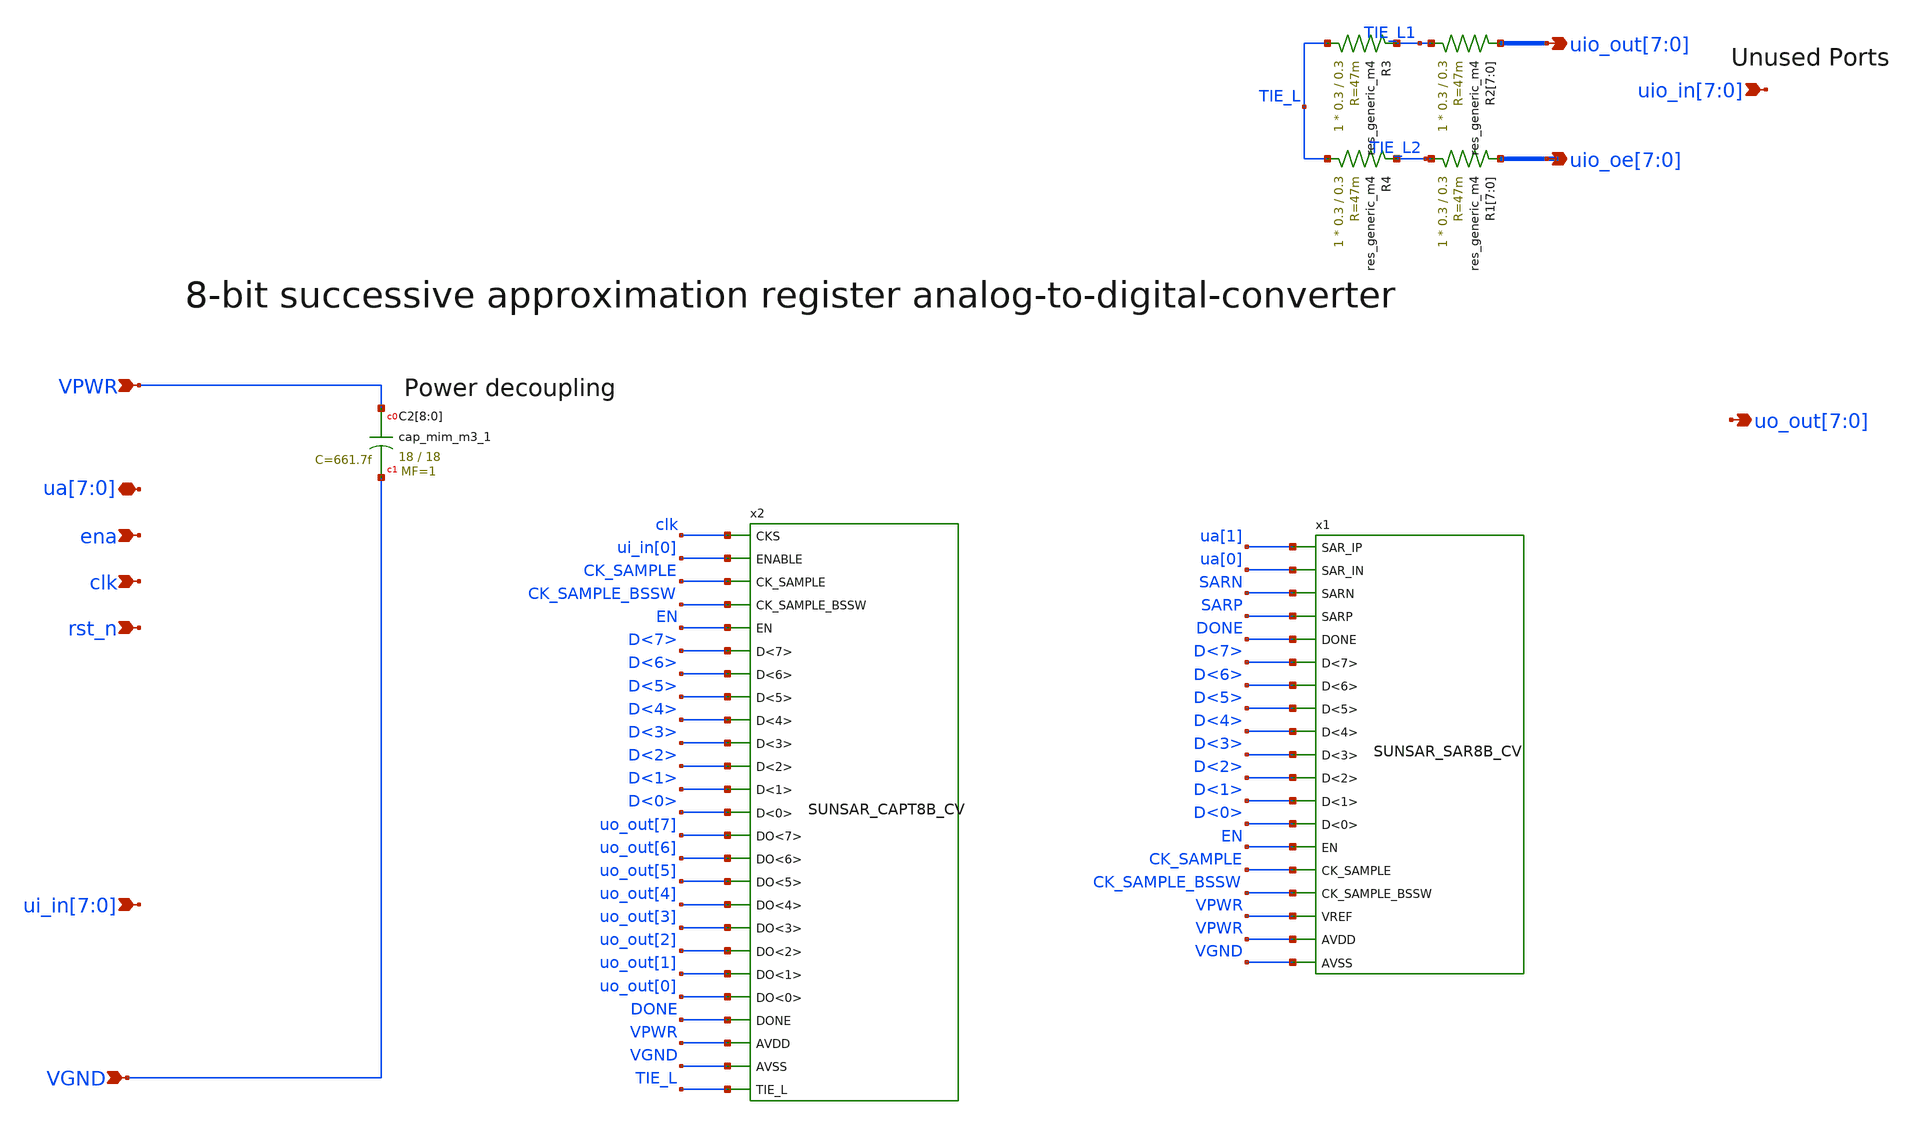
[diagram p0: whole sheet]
** sch_path: ip/tt06_sar_sky130nm/design/TT06_SAR_SKY130NM/tt_um_TT06_SAR_wulffern.sch
**.subckt tt_um_TT06_SAR_wulffern VPWR VGND
*+ ui_in[7],ui_in[6],ui_in[5],ui_in[4],ui_in[3],ui_in[2],ui_in[1],ui_in[0] uo_out[7],uo_out[6],uo_out[5],uo_out[4],uo_out[3],uo_out[2],uo_out[1],uo_out[0]
*+ uio_in[7],uio_in[6],uio_in[5],uio_in[4],uio_in[3],uio_in[2],uio_in[1],uio_in[0] uio_out[7],uio_out[6],uio_out[5],uio_out[4],uio_out[3],uio_out[2],uio_out[1],uio_out[0]
*+ uio_oe[7],uio_oe[6],uio_oe[5],uio_oe[4],uio_oe[3],uio_oe[2],uio_oe[1],uio_oe[0] ua[7],ua[6],ua[5],ua[4],ua[3],ua[2],ua[1],ua[0] ena clk rst_n
*.ipin VPWR
*.ipin VGND
*.ipin ui_in[7],ui_in[6],ui_in[5],ui_in[4],ui_in[3],ui_in[2],ui_in[1],ui_in[0]
*.opin uo_out[7],uo_out[6],uo_out[5],uo_out[4],uo_out[3],uo_out[2],uo_out[1],uo_out[0]
*.ipin uio_in[7],uio_in[6],uio_in[5],uio_in[4],uio_in[3],uio_in[2],uio_in[1],uio_in[0]
*.opin uio_out[7],uio_out[6],uio_out[5],uio_out[4],uio_out[3],uio_out[2],uio_out[1],uio_out[0]
*.opin uio_oe[7],uio_oe[6],uio_oe[5],uio_oe[4],uio_oe[3],uio_oe[2],uio_oe[1],uio_oe[0]
*.iopin ua[7],ua[6],ua[5],ua[4],ua[3],ua[2],ua[1],ua[0]
*.ipin ena
*.ipin clk
*.ipin rst_n
x1 ua[1] ua[0] SARN SARP DONE D<7> D<6> D<5> D<4> D<3> D<2> D<1> D<0> EN CK_SAMPLE CK_SAMPLE_BSSW
+ VPWR VPWR VGND SUNSAR_SAR8B_CV
x2 clk ui_in[0] CK_SAMPLE CK_SAMPLE_BSSW EN D<7> D<6> D<5> D<4> D<3> D<2> D<1> D<0> uo_out[7]
+ uo_out[6] uo_out[5] uo_out[4] uo_out[3] uo_out[2] uo_out[1] uo_out[0] DONE VPWR VGND TIE_L SUNSAR_CAPT8B_CV
R1[7] TIE_L2 uio_oe[7] sky130_fd_pr__res_generic_m4 W=0.3 L=0.3 m=1
R1[6] TIE_L2 uio_oe[6] sky130_fd_pr__res_generic_m4 W=0.3 L=0.3 m=1
R1[5] TIE_L2 uio_oe[5] sky130_fd_pr__res_generic_m4 W=0.3 L=0.3 m=1
R1[4] TIE_L2 uio_oe[4] sky130_fd_pr__res_generic_m4 W=0.3 L=0.3 m=1
R1[3] TIE_L2 uio_oe[3] sky130_fd_pr__res_generic_m4 W=0.3 L=0.3 m=1
R1[2] TIE_L2 uio_oe[2] sky130_fd_pr__res_generic_m4 W=0.3 L=0.3 m=1
R1[1] TIE_L2 uio_oe[1] sky130_fd_pr__res_generic_m4 W=0.3 L=0.3 m=1
R1[0] TIE_L2 uio_oe[0] sky130_fd_pr__res_generic_m4 W=0.3 L=0.3 m=1
R2[7] TIE_L1 uio_out[7] sky130_fd_pr__res_generic_m4 W=0.3 L=0.3 m=1
R2[6] TIE_L1 uio_out[6] sky130_fd_pr__res_generic_m4 W=0.3 L=0.3 m=1
R2[5] TIE_L1 uio_out[5] sky130_fd_pr__res_generic_m4 W=0.3 L=0.3 m=1
R2[4] TIE_L1 uio_out[4] sky130_fd_pr__res_generic_m4 W=0.3 L=0.3 m=1
R2[3] TIE_L1 uio_out[3] sky130_fd_pr__res_generic_m4 W=0.3 L=0.3 m=1
R2[2] TIE_L1 uio_out[2] sky130_fd_pr__res_generic_m4 W=0.3 L=0.3 m=1
R2[1] TIE_L1 uio_out[1] sky130_fd_pr__res_generic_m4 W=0.3 L=0.3 m=1
R2[0] TIE_L1 uio_out[0] sky130_fd_pr__res_generic_m4 W=0.3 L=0.3 m=1
R3 TIE_L TIE_L1 sky130_fd_pr__res_generic_m4 W=0.3 L=0.3 m=1
R4 TIE_L TIE_L2 sky130_fd_pr__res_generic_m4 W=0.3 L=0.3 m=1
XC2[8] VPWR VGND sky130_fd_pr__cap_mim_m3_1 W=18 L=18 MF=1 m=1
XC2[7] VPWR VGND sky130_fd_pr__cap_mim_m3_1 W=18 L=18 MF=1 m=1
XC2[6] VPWR VGND sky130_fd_pr__cap_mim_m3_1 W=18 L=18 MF=1 m=1
XC2[5] VPWR VGND sky130_fd_pr__cap_mim_m3_1 W=18 L=18 MF=1 m=1
XC2[4] VPWR VGND sky130_fd_pr__cap_mim_m3_1 W=18 L=18 MF=1 m=1
XC2[3] VPWR VGND sky130_fd_pr__cap_mim_m3_1 W=18 L=18 MF=1 m=1
XC2[2] VPWR VGND sky130_fd_pr__cap_mim_m3_1 W=18 L=18 MF=1 m=1
XC2[1] VPWR VGND sky130_fd_pr__cap_mim_m3_1 W=18 L=18 MF=1 m=1
XC2[0] VPWR VGND sky130_fd_pr__cap_mim_m3_1 W=18 L=18 MF=1 m=1
**.ends
.end
